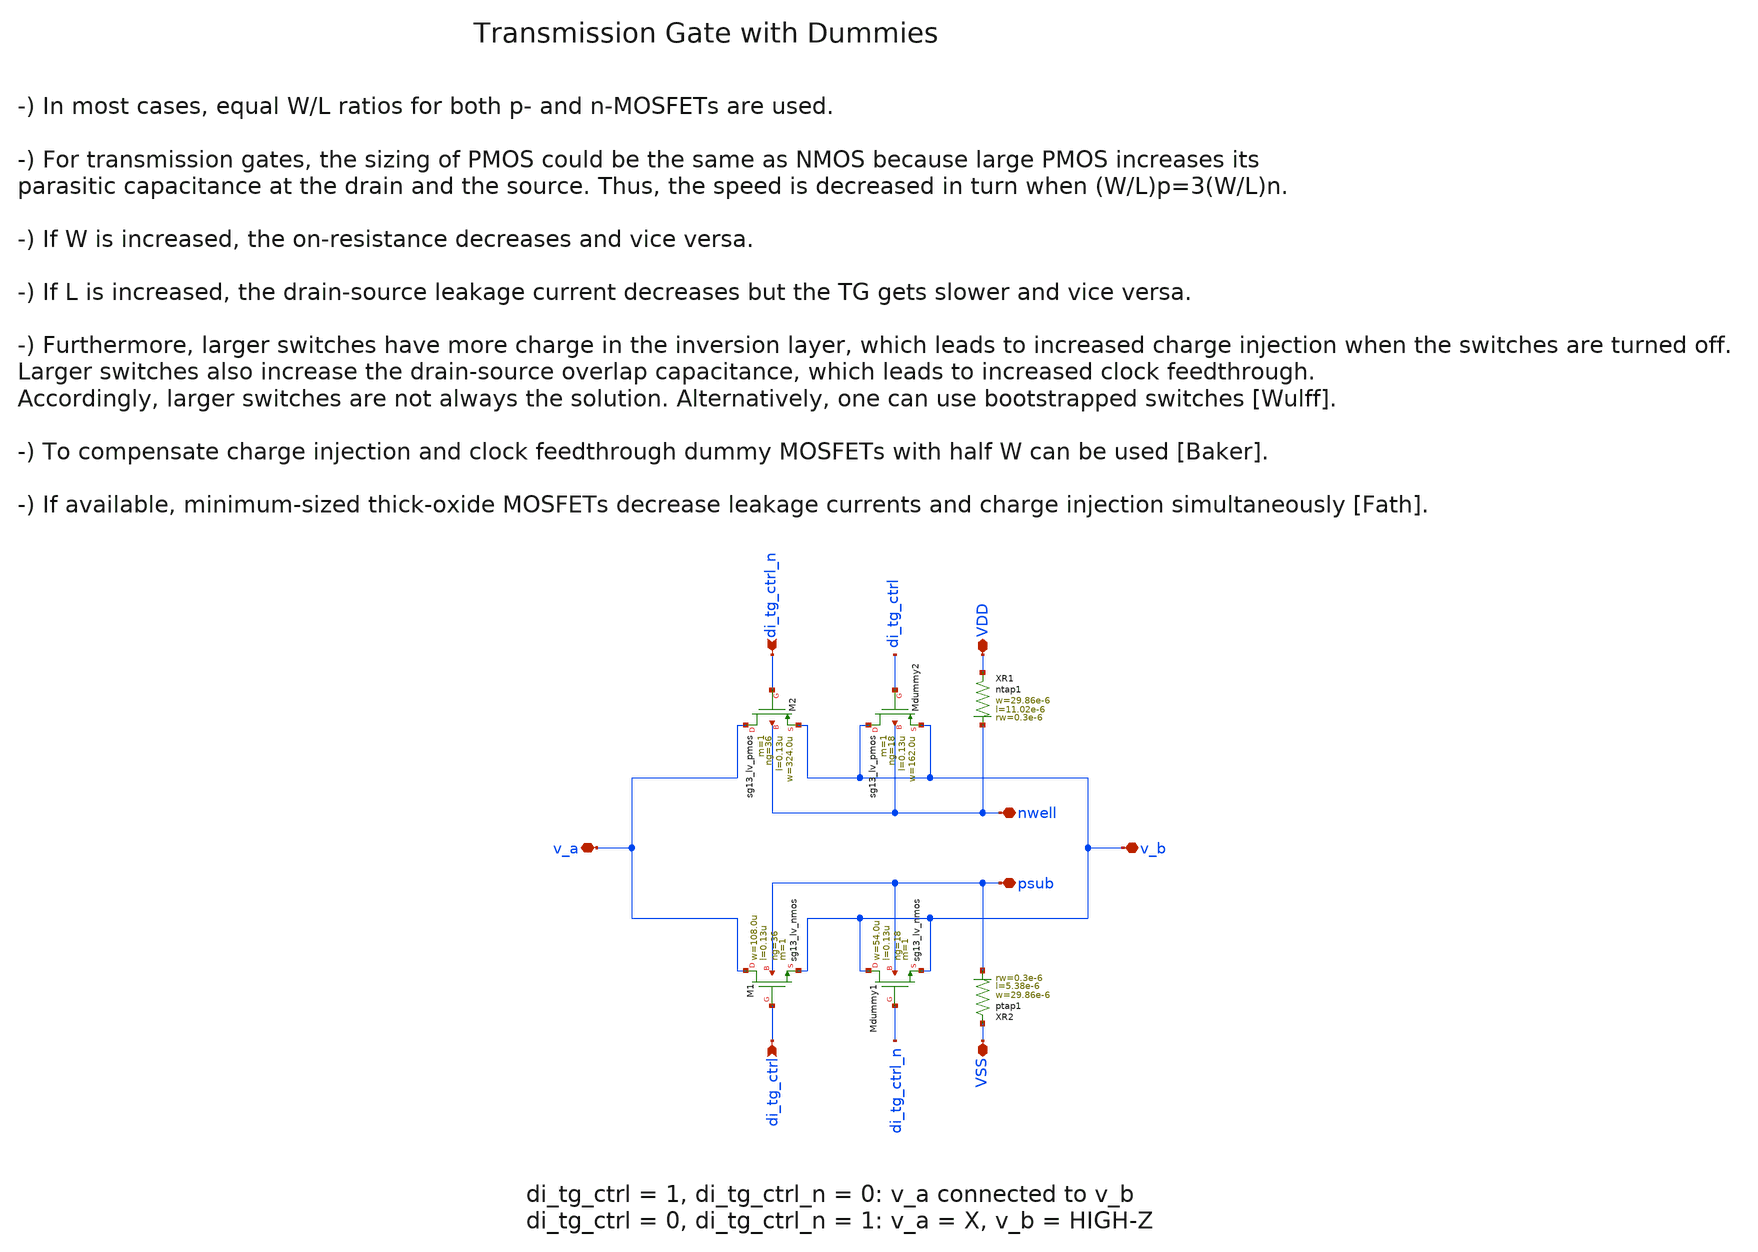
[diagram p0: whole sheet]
** sch_path: ihp130/macros/iqmod/xschem/iqmod_mixer_tg.sch
**.subckt iqmod_mixer_tg v_a v_b di_tg_ctrl di_tg_ctrl_n VDD VSS nwell psub
*.iopin v_a
*.iopin v_b
*.ipin di_tg_ctrl
*.ipin di_tg_ctrl_n
*.iopin VDD
*.iopin VSS
*.iopin nwell
*.iopin psub
XM1 v_a di_tg_ctrl v_b psub sg13_lv_nmos w=108.0u l=0.13u ng=36 m=1 mm_ok=1
XM2 v_a di_tg_ctrl_n v_b nwell sg13_lv_pmos w=324.0u l=0.13u ng=36 m=1 mm_ok=1
XMdummy2 v_b di_tg_ctrl v_b nwell sg13_lv_pmos w=162.0u l=0.13u ng=18 m=1 mm_ok=1
XMdummy1 v_b di_tg_ctrl_n v_b psub sg13_lv_nmos w=54.0u l=0.13u ng=18 m=1 mm_ok=1
XR1 VDD nwell ntap1 R=2.829 w=29.86e-6 l=11.02e-6 rw=0.3e-6
XR2 VSS psub ptap1 R=3.29 w=29.86e-6 l=5.38e-6 rw=0.3e-6
**.ends
.end
